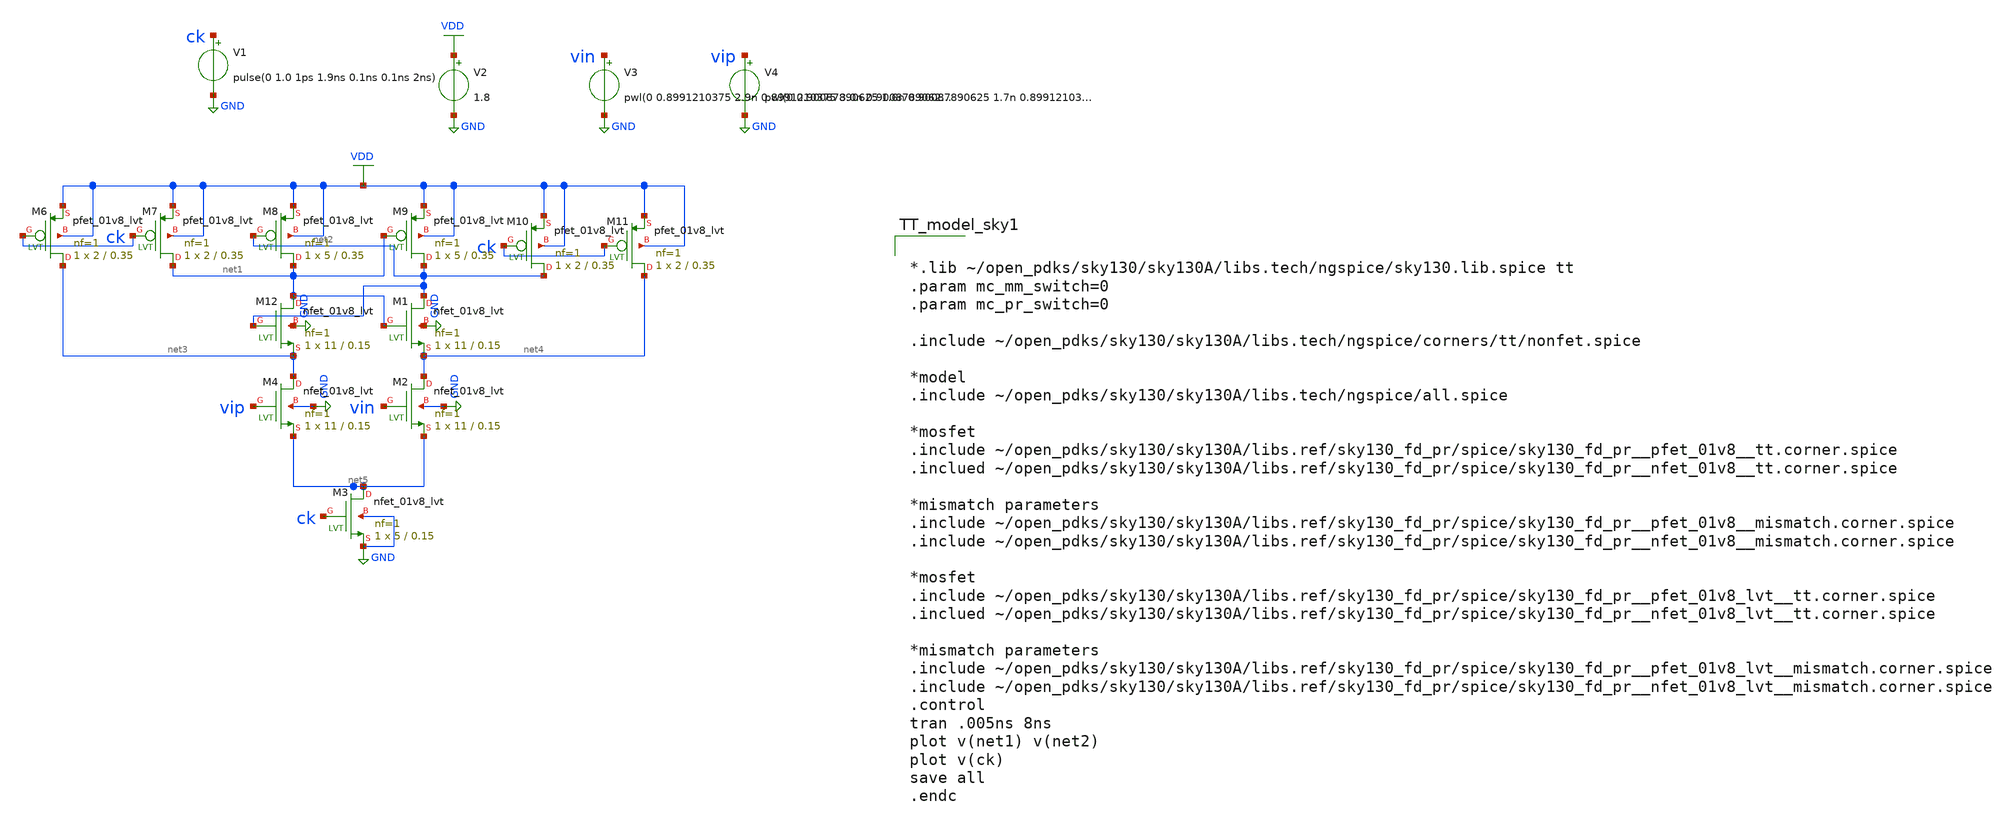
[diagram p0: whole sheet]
** sch_path: comparator.sch
**.subckt comparator
V1 ck GND pulse(0 1.0 1ps 1.9ns 0.1ns 0.1ns 2ns)
V2 VDD GND 1.8
V3 vin GND pwl(0 0.8991210375 2.9n 0.8991210375 3.0n 0.90087890625 4.9n 0.90087890625 5.0n
+ 0.8991210375)
V4 vip GND pwl(0 0.90087890625 1.6n 0.90087890625 1.7n 0.8991210375 3.6n 0.8991210375 3.7n
+ 0.90087890625)
XM12 net1 net2 net3 GND sky130_fd_pr__nfet_01v8_lvt L=0.15 W=11 nf=1 ad='int((nf+1)/2) * W/nf * 0.29'
+ as='int((nf+2)/2) * W/nf * 0.29' pd='2*int((nf+1)/2) * (W/nf + 0.29)' ps='2*int((nf+2)/2) * (W/nf + 0.29)'
+ nrd='0.29 / W' nrs='0.29 / W' sa=0 sb=0 sd=0 mult=1 m=1
XM1 net2 net1 net4 GND sky130_fd_pr__nfet_01v8_lvt L=0.15 W=11 nf=1 ad='int((nf+1)/2) * W/nf * 0.29'
+ as='int((nf+2)/2) * W/nf * 0.29' pd='2*int((nf+1)/2) * (W/nf + 0.29)' ps='2*int((nf+2)/2) * (W/nf + 0.29)'
+ nrd='0.29 / W' nrs='0.29 / W' sa=0 sb=0 sd=0 mult=1 m=1
XM2 net4 vin net5 GND sky130_fd_pr__nfet_01v8_lvt L=0.15 W=11 nf=1 ad='int((nf+1)/2) * W/nf * 0.29' as='int((nf+2)/2) * W/nf * 0.29'
+ pd='2*int((nf+1)/2) * (W/nf + 0.29)' ps='2*int((nf+2)/2) * (W/nf + 0.29)' nrd='0.29 / W' nrs='0.29 / W'
+ sa=0 sb=0 sd=0 mult=1 m=1
XM4 net3 vip net5 GND sky130_fd_pr__nfet_01v8_lvt L=0.15 W=11 nf=1 ad='int((nf+1)/2) * W/nf * 0.29' as='int((nf+2)/2) * W/nf * 0.29'
+ pd='2*int((nf+1)/2) * (W/nf + 0.29)' ps='2*int((nf+2)/2) * (W/nf + 0.29)' nrd='0.29 / W' nrs='0.29 / W'
+ sa=0 sb=0 sd=0 mult=1 m=1
XM3 net5 ck GND GND sky130_fd_pr__nfet_01v8_lvt L=0.15 W=5 nf=1 ad='int((nf+1)/2) * W/nf * 0.29' as='int((nf+2)/2) * W/nf * 0.29'
+ pd='2*int((nf+1)/2) * (W/nf + 0.29)' ps='2*int((nf+2)/2) * (W/nf + 0.29)' nrd='0.29 / W' nrs='0.29 / W'
+ sa=0 sb=0 sd=0 mult=1 m=1
XM6 net3 ck VDD VDD sky130_fd_pr__pfet_01v8_lvt L=0.35 W=2 nf=1 ad='int((nf+1)/2) * W/nf * 0.29' as='int((nf+2)/2) * W/nf * 0.29'
+ pd='2*int((nf+1)/2) * (W/nf + 0.29)' ps='2*int((nf+2)/2) * (W/nf + 0.29)' nrd='0.29 / W' nrs='0.29 / W'
+ sa=0 sb=0 sd=0 mult=1 m=1
XM7 net1 ck VDD VDD sky130_fd_pr__pfet_01v8_lvt L=0.35 W=2 nf=1 ad='int((nf+1)/2) * W/nf * 0.29' as='int((nf+2)/2) * W/nf * 0.29'
+ pd='2*int((nf+1)/2) * (W/nf + 0.29)' ps='2*int((nf+2)/2) * (W/nf + 0.29)' nrd='0.29 / W' nrs='0.29 / W'
+ sa=0 sb=0 sd=0 mult=1 m=1
XM8 net1 net2 VDD VDD sky130_fd_pr__pfet_01v8_lvt L=0.35 W=5 nf=1 ad='int((nf+1)/2) * W/nf * 0.29' as='int((nf+2)/2) * W/nf * 0.29'
+ pd='2*int((nf+1)/2) * (W/nf + 0.29)' ps='2*int((nf+2)/2) * (W/nf + 0.29)' nrd='0.29 / W' nrs='0.29 / W'
+ sa=0 sb=0 sd=0 mult=1 m=1
XM9 net2 net1 VDD VDD sky130_fd_pr__pfet_01v8_lvt L=0.35 W=5 nf=1 ad='int((nf+1)/2) * W/nf * 0.29' as='int((nf+2)/2) * W/nf * 0.29'
+ pd='2*int((nf+1)/2) * (W/nf + 0.29)' ps='2*int((nf+2)/2) * (W/nf + 0.29)' nrd='0.29 / W' nrs='0.29 / W'
+ sa=0 sb=0 sd=0 mult=1 m=1
XM10 net2 ck VDD VDD sky130_fd_pr__pfet_01v8_lvt L=0.35 W=2 nf=1 ad='int((nf+1)/2) * W/nf * 0.29' as='int((nf+2)/2) * W/nf * 0.29'
+ pd='2*int((nf+1)/2) * (W/nf + 0.29)' ps='2*int((nf+2)/2) * (W/nf + 0.29)' nrd='0.29 / W' nrs='0.29 / W'
+ sa=0 sb=0 sd=0 mult=1 m=1
XM11 net4 ck VDD VDD sky130_fd_pr__pfet_01v8_lvt L=0.35 W=2 nf=1 ad='int((nf+1)/2) * W/nf * 0.29' as='int((nf+2)/2) * W/nf * 0.29'
+ pd='2*int((nf+1)/2) * (W/nf + 0.29)' ps='2*int((nf+2)/2) * (W/nf + 0.29)' nrd='0.29 / W' nrs='0.29 / W'
+ sa=0 sb=0 sd=0 mult=1 m=1
**** begin user architecture code

*.lib ~/open_pdks/sky130/sky130A/libs.tech/ngspice/sky130.lib.spice tt
.param mc_mm_switch=0
.param mc_pr_switch=0

.include ~/open_pdks/sky130/sky130A/libs.tech/ngspice/corners/tt/nonfet.spice

*model
.include ~/open_pdks/sky130/sky130A/libs.tech/ngspice/all.spice

*mosfet
.include ~/open_pdks/sky130/sky130A/libs.ref/sky130_fd_pr/spice/sky130_fd_pr__pfet_01v8__tt.corner.spice
.inclued ~/open_pdks/sky130/sky130A/libs.ref/sky130_fd_pr/spice/sky130_fd_pr__nfet_01v8__tt.corner.spice

*mismatch parameters
.include ~/open_pdks/sky130/sky130A/libs.ref/sky130_fd_pr/spice/sky130_fd_pr__pfet_01v8__mismatch.corner.spice
.include ~/open_pdks/sky130/sky130A/libs.ref/sky130_fd_pr/spice/sky130_fd_pr__nfet_01v8__mismatch.corner.spice

*mosfet
.include ~/open_pdks/sky130/sky130A/libs.ref/sky130_fd_pr/spice/sky130_fd_pr__pfet_01v8_lvt__tt.corner.spice
.inclued ~/open_pdks/sky130/sky130A/libs.ref/sky130_fd_pr/spice/sky130_fd_pr__nfet_01v8_lvt__tt.corner.spice

*mismatch parameters
.include ~/open_pdks/sky130/sky130A/libs.ref/sky130_fd_pr/spice/sky130_fd_pr__pfet_01v8_lvt__mismatch.corner.spice
.include ~/open_pdks/sky130/sky130A/libs.ref/sky130_fd_pr/spice/sky130_fd_pr__nfet_01v8_lvt__mismatch.corner.spice
.control
tran .005ns 8ns
plot v(net1) v(net2)
plot v(ck)
save all
.endc

**** end user architecture code
**.ends
.GLOBAL GND
.GLOBAL VDD
.end
